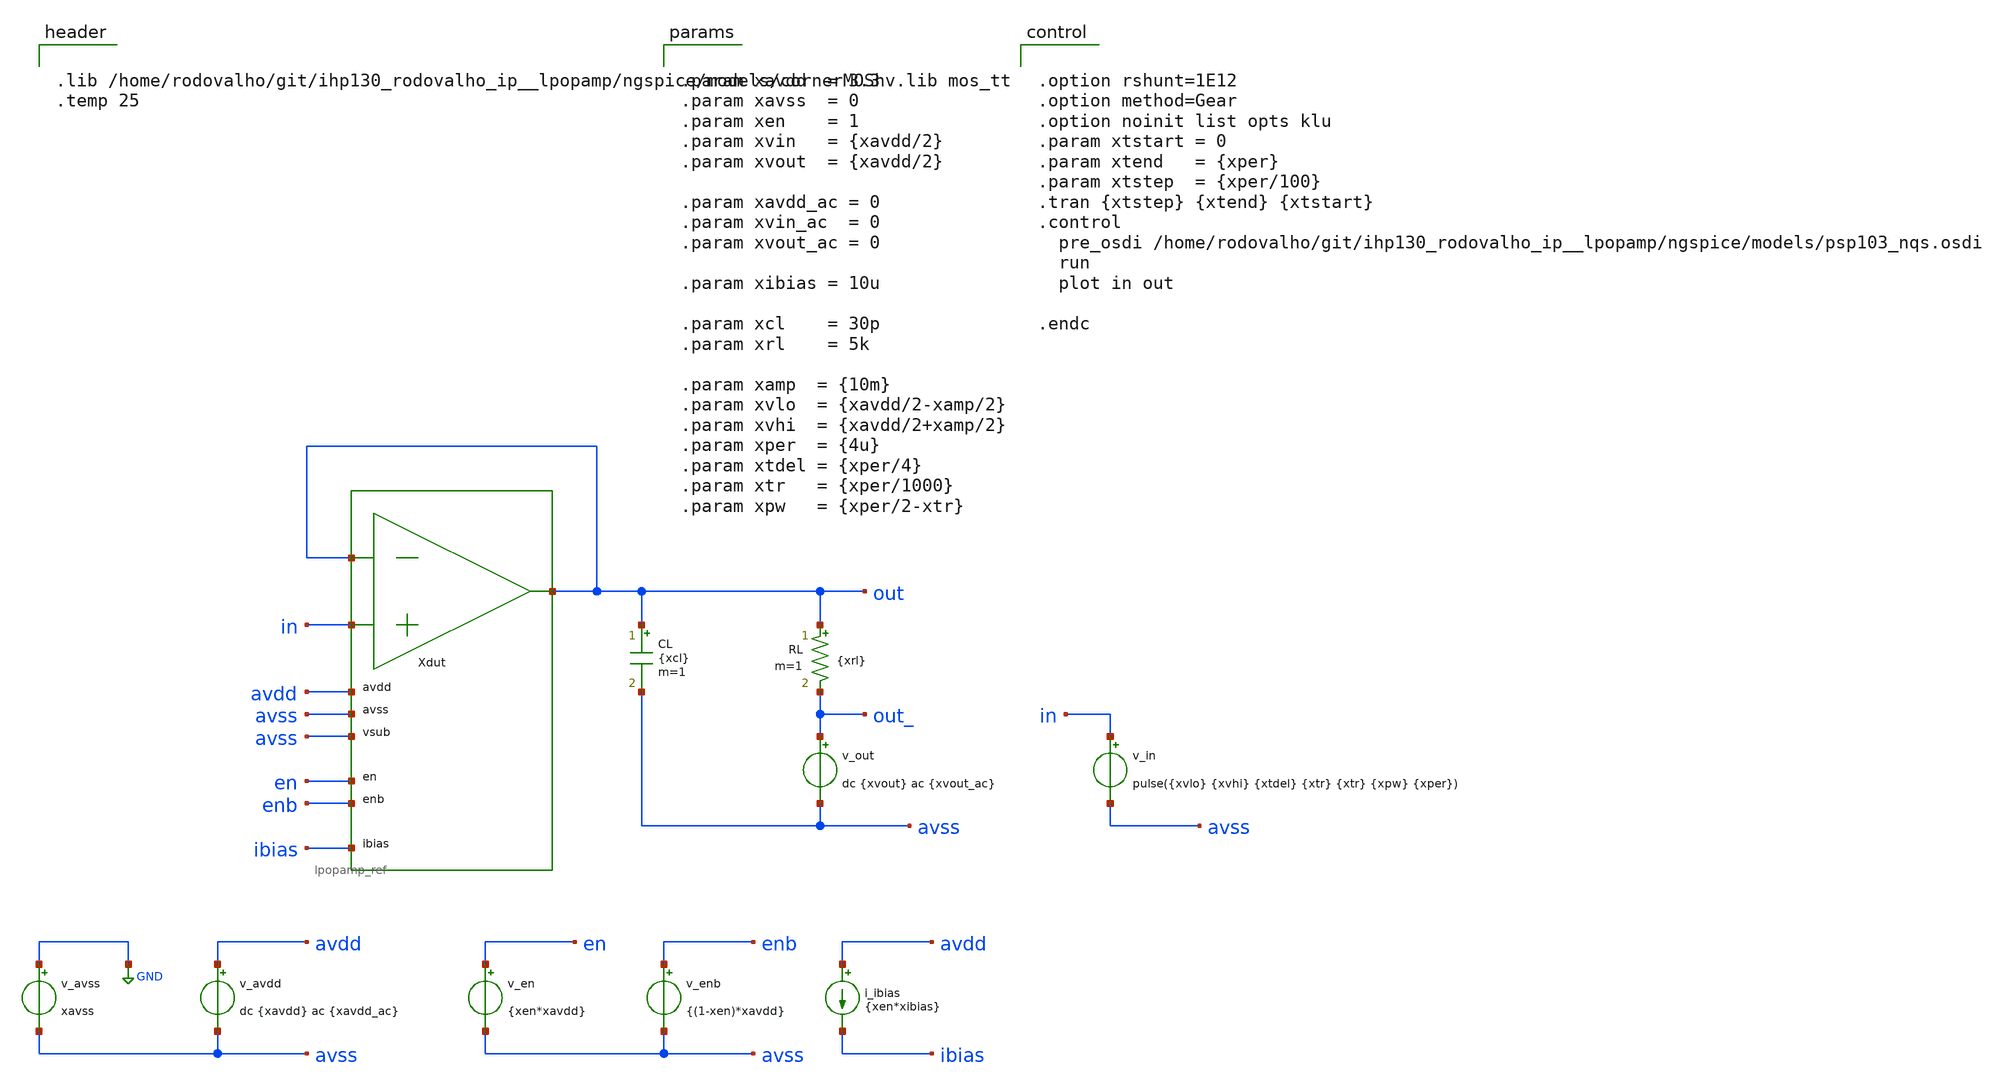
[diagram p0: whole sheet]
** sch_path: xschem/tb_lpopamp_buf_tran_step_small.sch
**.subckt tb_lpopamp_buf_tran_step_small
Xdut out in out avdd avss avss en enb ibias lpopamp_ref
v_avss GND avss xavss
v_avdd avdd avss dc {xavdd} ac {xavdd_ac}
v_in in avss pulse({xvlo} {xvhi} {xtdel} {xtr} {xtr} {xpw} {xper})
v_en en avss {xen*xavdd}
v_enb enb avss {(1-xen)*xavdd}
i_ibias avdd ibias {xen*xibias}
CL out avss {xcl} m=1
v_out out_ avss dc {xvout} ac {xvout_ac}
RL out out_ {xrl} m=1
**** begin user architecture code


.lib /home/rodovalho/git/ihp130_rodovalho_ip__lpopamp/ngspice/models/cornerMOShv.lib mos_tt
.temp 25




.option rshunt=1E12
.option method=Gear
.option noinit list opts klu
.param xtstart = 0
.param xtend   = {xper}
.param xtstep  = {xper/100}
.tran {xtstep} {xtend} {xtstart}
.control
  pre_osdi /home/rodovalho/git/ihp130_rodovalho_ip__lpopamp/ngspice/models/psp103_nqs.osdi
  run
  plot in out

.endc




.param xavdd  = 3.3
.param xavss  = 0
.param xen    = 1
.param xvin   = {xavdd/2}
.param xvout  = {xavdd/2}

.param xavdd_ac = 0
.param xvin_ac  = 0
.param xvout_ac = 0

.param xibias = 10u

.param xcl    = 30p
.param xrl    = 5k

.param xamp  = {10m}
.param xvlo  = {xavdd/2-xamp/2}
.param xvhi  = {xavdd/2+xamp/2}
.param xper  = {4u}
.param xtdel = {xper/4}
.param xtr   = {xper/1000}
.param xpw   = {xper/2-xtr}


**** end user architecture code
**.ends
.GLOBAL GND
.end
